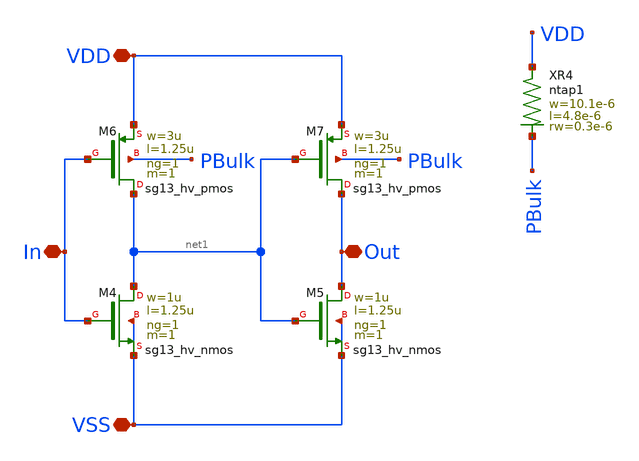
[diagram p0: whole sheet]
** sch_path: LVS/LVS_Sch/Buffer.sch
**.subckt Buffer In Out VDD VSS
*.iopin In
*.iopin Out
*.iopin VDD
*.iopin VSS
XM4 net1 In VSS VSS sg13_hv_nmos w=1u l=1.25u ng=1 m=1 mm_ok=1
XM5 Out net1 VSS VSS sg13_hv_nmos w=1u l=1.25u ng=1 m=1 mm_ok=1
XM6 net1 In VDD PBulk sg13_hv_pmos w=3u l=1.25u ng=1 m=1 mm_ok=1
XM7 Out net1 VDD PBulk sg13_hv_pmos w=3u l=1.25u ng=1 m=1 mm_ok=1
XR4 VDD PBulk ntap1 R=7.969 w=10.1e-6 l=4.8e-6 rw=0.3e-6
**.ends
.end
